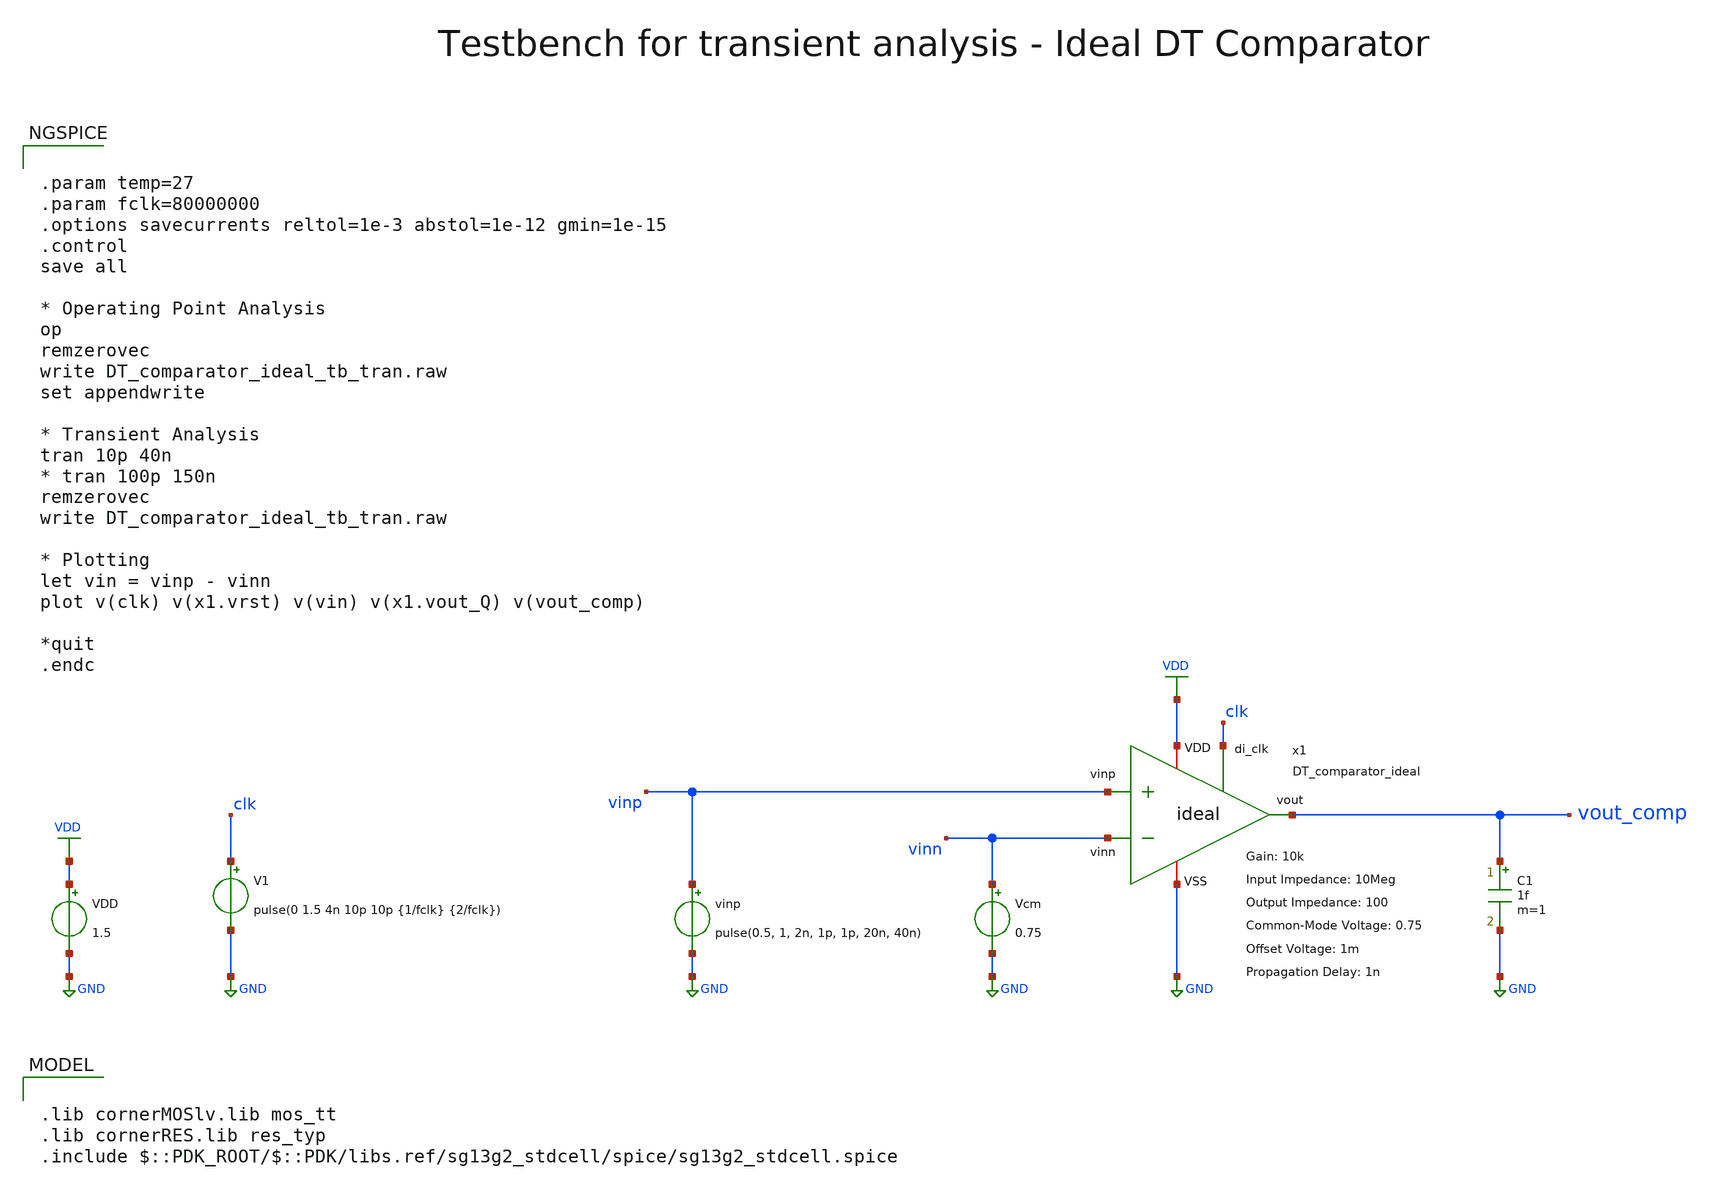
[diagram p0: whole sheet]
** sch_path: SG13G2_ATBS-ADC-main/xschem/comparator/discrete_time/ideal/testbenches/DT_comparator_ideal_tb_tran.sch
**.subckt DT_comparator_ideal_tb_tran
C1 vout_comp GND 1f m=1
Vcm vinn GND 0.75
VDD VDD GND 1.5
x1 vinp vinn VDD vout_comp GND clk DT_comparator_ideal A=10k Rin=10Meg Rout=100 Pdc= Vcm=0.75
+ Voffs=1m tpd=1n
V1 clk GND pulse(0 1.5 4n 10p 10p {1/fclk} {2/fclk})
vinp vinp GND pulse(0.5, 1, 2n, 1p, 1p, 20n, 40n)
**** begin user architecture code

.lib cornerMOSlv.lib mos_tt
.lib cornerRES.lib res_typ
.include $::PDK_ROOT/$::PDK/libs.ref/sg13g2_stdcell/spice/sg13g2_stdcell.spice



.param temp=27
.param fclk=80000000
.options savecurrents reltol=1e-3 abstol=1e-12 gmin=1e-15
.control
save all

* Operating Point Analysis
op
remzerovec
write DT_comparator_ideal_tb_tran.raw
set appendwrite

* Transient Analysis
tran 10p 40n
* tran 100p 150n
remzerovec
write DT_comparator_ideal_tb_tran.raw

* Plotting
let vin = vinp - vinn
plot v(clk) v(x1.vrst) v(vin) v(x1.vout_Q) v(vout_comp)

*quit
.endc

**** end user architecture code
**.ends

* expanding   symbol:  comparator/discrete_time/ideal/DT_comparator_ideal.sym # of pins=6
** sym_path: SG13G2_ATBS-ADC-main/xschem/comparator/discrete_time/ideal/DT_comparator_ideal.sym
** sch_path: SG13G2_ATBS-ADC-main/xschem/comparator/discrete_time/ideal/DT_comparator_ideal.sch
.subckt DT_comparator_ideal vinp vinn VDD vout VSS di_clk  A=10k Rin=10Meg Rout=100 Vcm=0.75
+ Voffs=1m tpd=1n
*.ipin vinn
*.opin vout
*.ipin vinp
*.iopin VSS
*.iopin VDD
*.ipin di_clk
R1 vinp vinn {Rin} m=1
B1 net1 VSS v=v(VDD)/2*tanh({A}/(v(VDD)/2)*(v(vinp)-v(vinn)-{Voffs}))+{Vcm}
R3 vout net3 {Rout} m=1
* noconn #net2
vrst vrst VSS pulse(1.5, 0, 0, 1p, 1p, 100p, 200p, 1)
* noconn VDD
x1 vout_Q net2 di_clk net1 vrst VDD VSS sg13g2_dfrbp_1
A1 vout_Q net3 VSS del_subckt
.model del_subckt delay(delay=tpd buffer_size=8192)
.ends


* expanding   symbol:  sg13g2_stdcells/sg13g2_dfrbp_1.sym # of pins=5
** sym_path: sg13g2_stdcells/sg13g2_dfrbp_1.sym
** sch_path: sg13g2_stdcells/sg13g2_dfrbp_1.sch
.subckt sg13g2_dfrbp_1 Q Q_N CLK D RESET_B VDD VSS
*.ipin D
*.ipin RESET_B
*.ipin CLK
*.opin Q
*.opin Q_N
*.iopin VDD
*.iopin VSS
XM1 Db D net10 VSS sg13_lv_nmos w=420.00n l=130.00n ng=1 m=1 mm_ok=1
XM2 net10 RESET_B VSS VSS sg13_lv_nmos w=420.00n l=130.00n ng=1 m=1 mm_ok=1
XM3 net1 clkneg net9 VSS sg13_lv_nmos w=420.00n l=130.00n ng=1 m=1 mm_ok=1
XM4 net9 net1 VSS VSS sg13_lv_nmos w=420.00n l=130.00n ng=1 m=1 mm_ok=1
XM5 net1 net1 net5 VSS sg13_lv_nmos w=420.00n l=130.00n ng=1 m=1 mm_ok=1
XM6 net5 RESET_B VSS VSS sg13_lv_nmos w=420.00n l=130.00n ng=1 m=1 mm_ok=1
XM7 Q_N net1 VSS VSS sg13_lv_nmos w=740.00n l=130.00n ng=1 m=1 mm_ok=1
XM8 net2 net1 VSS VSS sg13_lv_nmos w=740.00n l=130.00n ng=1 m=1 mm_ok=1
XM9 Q net2 VSS VSS sg13_lv_nmos w=740.00n l=130.00n ng=1 m=1 mm_ok=1
XM10 clkneg CLK VSS VSS sg13_lv_nmos w=740.00n l=130.00n ng=1 m=1 mm_ok=1
XM11 clkpos clkneg VSS VSS sg13_lv_nmos w=740.00n l=130.00n ng=1 m=1 mm_ok=1
XM12 Db clkneg net3 VSS sg13_lv_nmos w=420.00n l=130.00n ng=1 m=1 mm_ok=1
XM13 net3 clkpos net8 VSS sg13_lv_nmos w=420.00n l=130.00n ng=1 m=1 mm_ok=1
XM14 net8 net3 net4 VSS sg13_lv_nmos w=420.00n l=130.00n ng=1 m=1 mm_ok=1
XM15 net4 RESET_B VSS VSS sg13_lv_nmos w=420.00n l=130.00n ng=1 m=1 mm_ok=1
XM16 net3 net3 VSS VSS sg13_lv_nmos w=740.00n l=130.00n ng=1 m=1 mm_ok=1
XM17 net3 clkpos net1 VSS sg13_lv_nmos w=740.00n l=130.00n ng=1 m=1 mm_ok=1
XM18 Db RESET_B VDD VDD sg13_lv_pmos w=420.00n l=130.00n ng=1 m=1 mm_ok=1
XM19 Db D VDD VDD sg13_lv_pmos w=420.00n l=130.00n ng=1 m=1 mm_ok=1
XM20 net7 net1 VDD VDD sg13_lv_pmos w=420.00n l=130.00n ng=1 m=1 mm_ok=1
XM21 net1 clkpos net7 VDD sg13_lv_pmos w=420.00n l=130.00n ng=1 m=1 mm_ok=1
XM22 net1 net1 VDD VDD sg13_lv_pmos w=420.00n l=130.00n ng=1 m=1 mm_ok=1
XM23 net1 RESET_B VDD VDD sg13_lv_pmos w=420.00n l=130.00n ng=1 m=1 mm_ok=1
XM24 Q_N net1 VDD VDD sg13_lv_pmos w=1.12u l=130.00n ng=1 m=1 mm_ok=1
XM25 net2 net1 VDD VDD sg13_lv_pmos w=1.12u l=130.00n ng=1 m=1 mm_ok=1
XM26 Q net2 VDD VDD sg13_lv_pmos w=1.12u l=130.00n ng=1 m=1 mm_ok=1
XM27 clkneg CLK VDD VDD sg13_lv_pmos w=1.12u l=130.00n ng=1 m=1 mm_ok=1
XM28 clkpos clkneg VDD VDD sg13_lv_pmos w=1.12u l=130.00n ng=1 m=1 mm_ok=1
XM29 Db clkpos net3 VDD sg13_lv_pmos w=420.00n l=130.00n ng=1 m=1 mm_ok=1
XM30 net6 net3 VDD VDD sg13_lv_pmos w=420.00n l=130.00n ng=1 m=1 mm_ok=1
XM31 net3 clkneg net6 VDD sg13_lv_pmos w=420.00n l=130.00n ng=1 m=1 mm_ok=1
XM32 net3 RESET_B VDD VDD sg13_lv_pmos w=420.00n l=130.00n ng=1 m=1 mm_ok=1
XM33 net3 net3 VDD VDD sg13_lv_pmos w=1.000u l=130.00n ng=1 m=1 mm_ok=1
XM34 net3 clkneg net1 VDD sg13_lv_pmos w=1.000u l=130.00n ng=1 m=1 mm_ok=1
.ends

.GLOBAL VDD
.GLOBAL GND
.end
